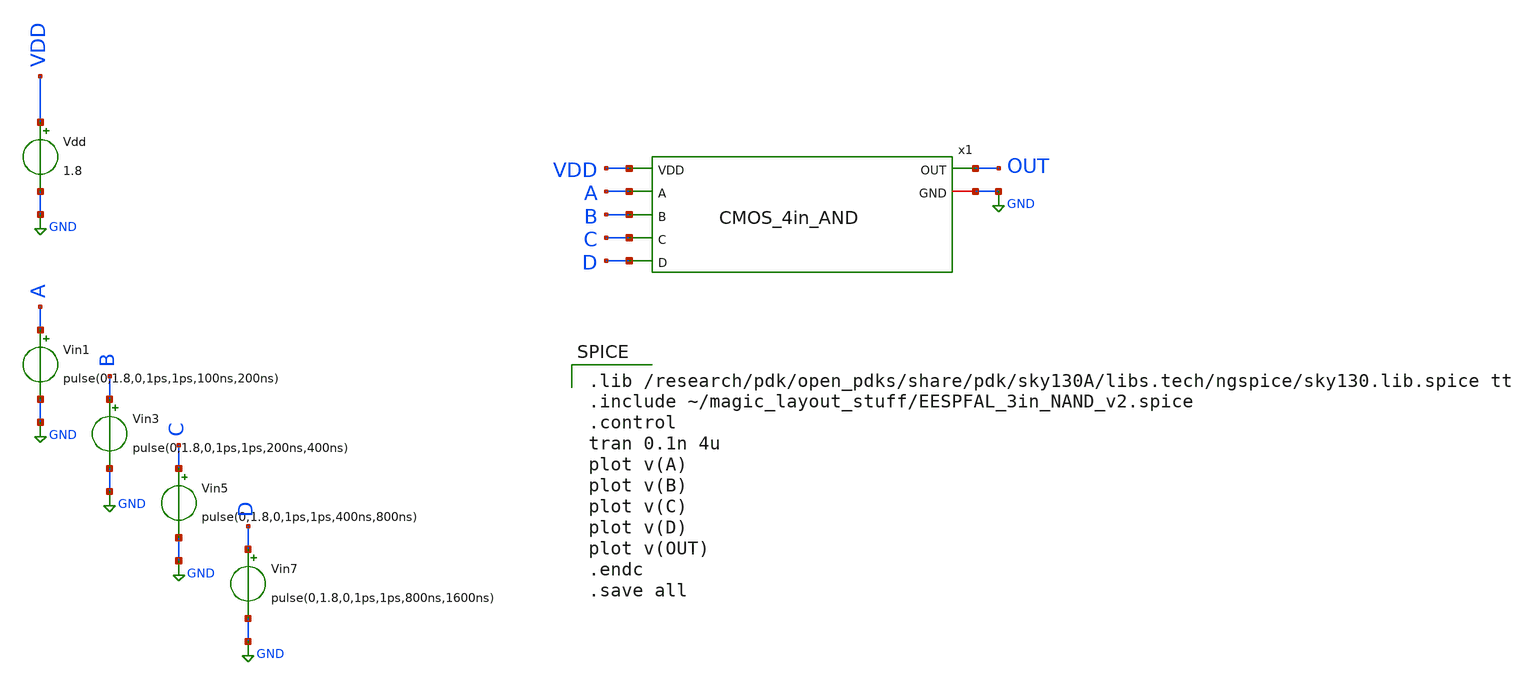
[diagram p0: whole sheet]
** sch_path: skywater_stuff/untitled-7.sch
**.subckt untitled-7
Vin1 A GND pulse(0,1.8,0,1ps,1ps,100ns,200ns)
Vin3 B GND pulse(0,1.8,0,1ps,1ps,200ns,400ns)
Vin5 C GND pulse(0,1.8,0,1ps,1ps,400ns,800ns)
Vin7 D GND pulse(0,1.8,0,1ps,1ps,800ns,1600ns)
x1 A B C D OUT GND VDD CMOS_4in_AND
Vdd VDD GND 1.8
**** begin user architecture code

.lib /research/pdk/open_pdks/share/pdk/sky130A/libs.tech/ngspice/sky130.lib.spice tt
.include ~/magic_layout_stuff/EESPFAL_3in_NAND_v2.spice
.control
tran 0.1n 4u
plot v(A)
plot v(B)
plot v(C)
plot v(D)
plot v(OUT)
.endc
.save all

**** end user architecture code
**.ends

* expanding   symbol:  CMOS_4in_AND.sym # of pins=7
** sym_path: skywater_stuff/CMOS_4in_AND.sym
** sch_path: skywater_stuff/CMOS_4in_AND.sch
.subckt CMOS_4in_AND A B C D OUT GND VDD
*.ipin A
*.ipin B
*.ipin C
*.ipin D
*.opin OUT
*.iopin GND
*.ipin VDD
XM3 net1 B VDD VDD sky130_fd_pr__pfet_01v8 L=0.15 W=3 nf=1 ad='int((nf+1)/2) * W/nf * 0.29' as='int((nf+2)/2) * W/nf * 0.29'
+ pd='2*int((nf+1)/2) * (W/nf + 0.29)' ps='2*int((nf+2)/2) * (W/nf + 0.29)' nrd='0.29 / W' nrs='0.29 / W'
+ sa=0 sb=0 sd=0 mult=1 m=1
XM4 net1 C VDD VDD sky130_fd_pr__pfet_01v8 L=0.15 W=3 nf=1 ad='int((nf+1)/2) * W/nf * 0.29' as='int((nf+2)/2) * W/nf * 0.29'
+ pd='2*int((nf+1)/2) * (W/nf + 0.29)' ps='2*int((nf+2)/2) * (W/nf + 0.29)' nrd='0.29 / W' nrs='0.29 / W'
+ sa=0 sb=0 sd=0 mult=1 m=1
XM6 net2 B net3 GND sky130_fd_pr__nfet_01v8 L=0.15 W=1.5 nf=1 ad='int((nf+1)/2) * W/nf * 0.29' as='int((nf+2)/2) * W/nf * 0.29'
+ pd='2*int((nf+1)/2) * (W/nf + 0.29)' ps='2*int((nf+2)/2) * (W/nf + 0.29)' nrd='0.29 / W' nrs='0.29 / W'
+ sa=0 sb=0 sd=0 mult=1 m=1
XM7 net3 C net4 GND sky130_fd_pr__nfet_01v8 L=0.15 W=1.5 nf=1 ad='int((nf+1)/2) * W/nf * 0.29' as='int((nf+2)/2) * W/nf * 0.29'
+ pd='2*int((nf+1)/2) * (W/nf + 0.29)' ps='2*int((nf+2)/2) * (W/nf + 0.29)' nrd='0.29 / W' nrs='0.29 / W'
+ sa=0 sb=0 sd=0 mult=1 m=1
XM8 net4 D GND GND sky130_fd_pr__nfet_01v8 L=0.15 W=1.5 nf=1 ad='int((nf+1)/2) * W/nf * 0.29' as='int((nf+2)/2) * W/nf * 0.29'
+ pd='2*int((nf+1)/2) * (W/nf + 0.29)' ps='2*int((nf+2)/2) * (W/nf + 0.29)' nrd='0.29 / W' nrs='0.29 / W'
+ sa=0 sb=0 sd=0 mult=1 m=1
XM9 OUT net1 GND GND sky130_fd_pr__nfet_01v8 L=0.15 W=1.5 nf=1 ad='int((nf+1)/2) * W/nf * 0.29' as='int((nf+2)/2) * W/nf * 0.29'
+ pd='2*int((nf+1)/2) * (W/nf + 0.29)' ps='2*int((nf+2)/2) * (W/nf + 0.29)' nrd='0.29 / W' nrs='0.29 / W'
+ sa=0 sb=0 sd=0 mult=1 m=1
XM10 OUT net1 VDD VDD sky130_fd_pr__pfet_01v8 L=0.15 W=3 nf=1 ad='int((nf+1)/2) * W/nf * 0.29' as='int((nf+2)/2) * W/nf * 0.29'
+ pd='2*int((nf+1)/2) * (W/nf + 0.29)' ps='2*int((nf+2)/2) * (W/nf + 0.29)' nrd='0.29 / W' nrs='0.29 / W'
+ sa=0 sb=0 sd=0 mult=1 m=1
XM1 net1 A net2 GND sky130_fd_pr__nfet_01v8 L=0.15 W=1.5 nf=1 ad='int((nf+1)/2) * W/nf * 0.29' as='int((nf+2)/2) * W/nf * 0.29'
+ pd='2*int((nf+1)/2) * (W/nf + 0.29)' ps='2*int((nf+2)/2) * (W/nf + 0.29)' nrd='0.29 / W' nrs='0.29 / W'
+ sa=0 sb=0 sd=0 mult=1 m=1
XM2 net1 A VDD VDD sky130_fd_pr__pfet_01v8 L=0.15 W=3 nf=1 ad='int((nf+1)/2) * W/nf * 0.29' as='int((nf+2)/2) * W/nf * 0.29'
+ pd='2*int((nf+1)/2) * (W/nf + 0.29)' ps='2*int((nf+2)/2) * (W/nf + 0.29)' nrd='0.29 / W' nrs='0.29 / W'
+ sa=0 sb=0 sd=0 mult=1 m=1
XM5 net1 D VDD VDD sky130_fd_pr__pfet_01v8 L=0.15 W=3 nf=1 ad='int((nf+1)/2) * W/nf * 0.29' as='int((nf+2)/2) * W/nf * 0.29'
+ pd='2*int((nf+1)/2) * (W/nf + 0.29)' ps='2*int((nf+2)/2) * (W/nf + 0.29)' nrd='0.29 / W' nrs='0.29 / W'
+ sa=0 sb=0 sd=0 mult=1 m=1
.ends

.GLOBAL GND
.end
